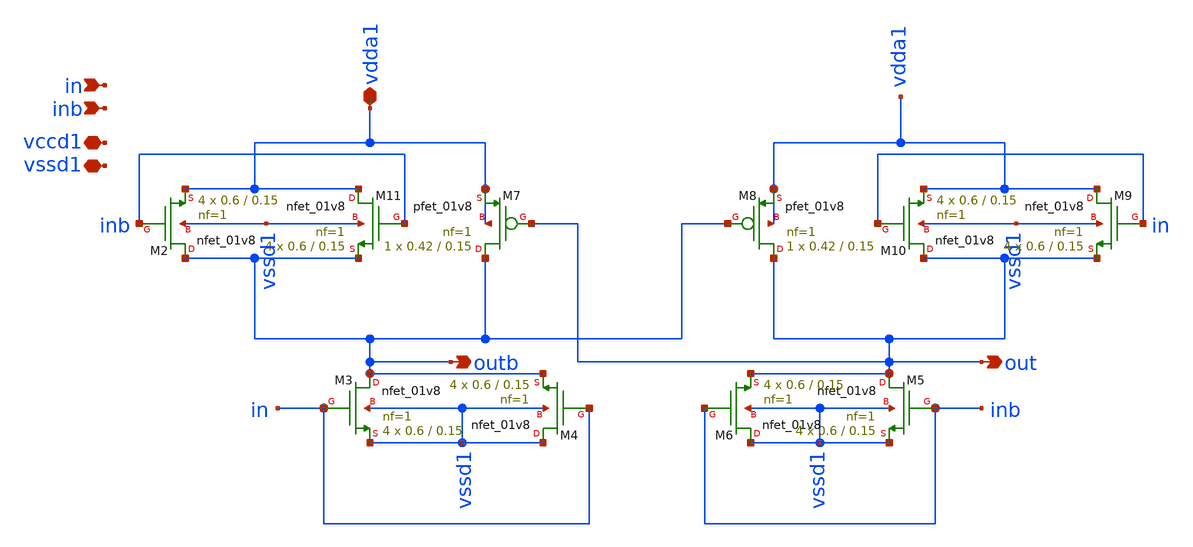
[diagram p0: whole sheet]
** sch_path: xschem/level_shifter/level_up_shifter_no_inv.sch
**.subckt level_up_shifter_no_inv in vdda1 out outb inb vssd1 vccd1
*.ipin in
*.iopin vdda1
*.opin out
*.opin outb
*.ipin inb
*.iopin vssd1
*.iopin vccd1
XM7 outb out vdda1 vdda1 sky130_fd_pr__pfet_01v8 L=0.15 W=0.42 nf=1 ad='int((nf+1)/2) * W/nf * 0.29'
+ as='int((nf+2)/2) * W/nf * 0.29' pd='2*int((nf+1)/2) * (W/nf + 0.29)' ps='2*int((nf+2)/2) * (W/nf + 0.29)'
+ nrd='0.29 / W' nrs='0.29 / W' sa=0 sb=0 sd=0 mult=1 m=1
XM8 out outb vdda1 vdda1 sky130_fd_pr__pfet_01v8 L=0.15 W=0.42 nf=1 ad='int((nf+1)/2) * W/nf * 0.29'
+ as='int((nf+2)/2) * W/nf * 0.29' pd='2*int((nf+1)/2) * (W/nf + 0.29)' ps='2*int((nf+2)/2) * (W/nf + 0.29)'
+ nrd='0.29 / W' nrs='0.29 / W' sa=0 sb=0 sd=0 mult=1 m=1
XM2 outb inb vdda1 vssd1 sky130_fd_pr__nfet_01v8 L=0.15 W=0.6 nf=1 ad='int((nf+1)/2) * W/nf * 0.29' as='int((nf+2)/2) * W/nf * 0.29'
+ pd='2*int((nf+1)/2) * (W/nf + 0.29)' ps='2*int((nf+2)/2) * (W/nf + 0.29)' nrd='0.29 / W' nrs='0.29 / W'
+ sa=0 sb=0 sd=0 mult=4 m=4
XM3 outb in vssd1 vssd1 sky130_fd_pr__nfet_01v8 L=0.15 W=0.6 nf=1 ad='int((nf+1)/2) * W/nf * 0.29' as='int((nf+2)/2) * W/nf * 0.29'
+ pd='2*int((nf+1)/2) * (W/nf + 0.29)' ps='2*int((nf+2)/2) * (W/nf + 0.29)' nrd='0.29 / W' nrs='0.29 / W'
+ sa=0 sb=0 sd=0 mult=4 m=4
XM4 vssd1 in outb vssd1 sky130_fd_pr__nfet_01v8 L=0.15 W=0.6 nf=1 ad='int((nf+1)/2) * W/nf * 0.29' as='int((nf+2)/2) * W/nf * 0.29'
+ pd='2*int((nf+1)/2) * (W/nf + 0.29)' ps='2*int((nf+2)/2) * (W/nf + 0.29)' nrd='0.29 / W' nrs='0.29 / W'
+ sa=0 sb=0 sd=0 mult=4 m=4
XM5 out inb vssd1 vssd1 sky130_fd_pr__nfet_01v8 L=0.15 W=0.6 nf=1 ad='int((nf+1)/2) * W/nf * 0.29' as='int((nf+2)/2) * W/nf * 0.29'
+ pd='2*int((nf+1)/2) * (W/nf + 0.29)' ps='2*int((nf+2)/2) * (W/nf + 0.29)' nrd='0.29 / W' nrs='0.29 / W'
+ sa=0 sb=0 sd=0 mult=4 m=4
XM6 vssd1 inb out vssd1 sky130_fd_pr__nfet_01v8 L=0.15 W=0.6 nf=1 ad='int((nf+1)/2) * W/nf * 0.29' as='int((nf+2)/2) * W/nf * 0.29'
+ pd='2*int((nf+1)/2) * (W/nf + 0.29)' ps='2*int((nf+2)/2) * (W/nf + 0.29)' nrd='0.29 / W' nrs='0.29 / W'
+ sa=0 sb=0 sd=0 mult=4 m=4
XM9 vdda1 in out vssd1 sky130_fd_pr__nfet_01v8 L=0.15 W=0.6 nf=1 ad='int((nf+1)/2) * W/nf * 0.29' as='int((nf+2)/2) * W/nf * 0.29'
+ pd='2*int((nf+1)/2) * (W/nf + 0.29)' ps='2*int((nf+2)/2) * (W/nf + 0.29)' nrd='0.29 / W' nrs='0.29 / W'
+ sa=0 sb=0 sd=0 mult=4 m=4
XM10 out in vdda1 vssd1 sky130_fd_pr__nfet_01v8 L=0.15 W=0.6 nf=1 ad='int((nf+1)/2) * W/nf * 0.29' as='int((nf+2)/2) * W/nf * 0.29'
+ pd='2*int((nf+1)/2) * (W/nf + 0.29)' ps='2*int((nf+2)/2) * (W/nf + 0.29)' nrd='0.29 / W' nrs='0.29 / W'
+ sa=0 sb=0 sd=0 mult=4 m=4
XM11 vdda1 inb outb vssd1 sky130_fd_pr__nfet_01v8 L=0.15 W=0.6 nf=1 ad='int((nf+1)/2) * W/nf * 0.29'
+ as='int((nf+2)/2) * W/nf * 0.29' pd='2*int((nf+1)/2) * (W/nf + 0.29)' ps='2*int((nf+2)/2) * (W/nf + 0.29)'
+ nrd='0.29 / W' nrs='0.29 / W' sa=0 sb=0 sd=0 mult=4 m=4
**.ends
.end
